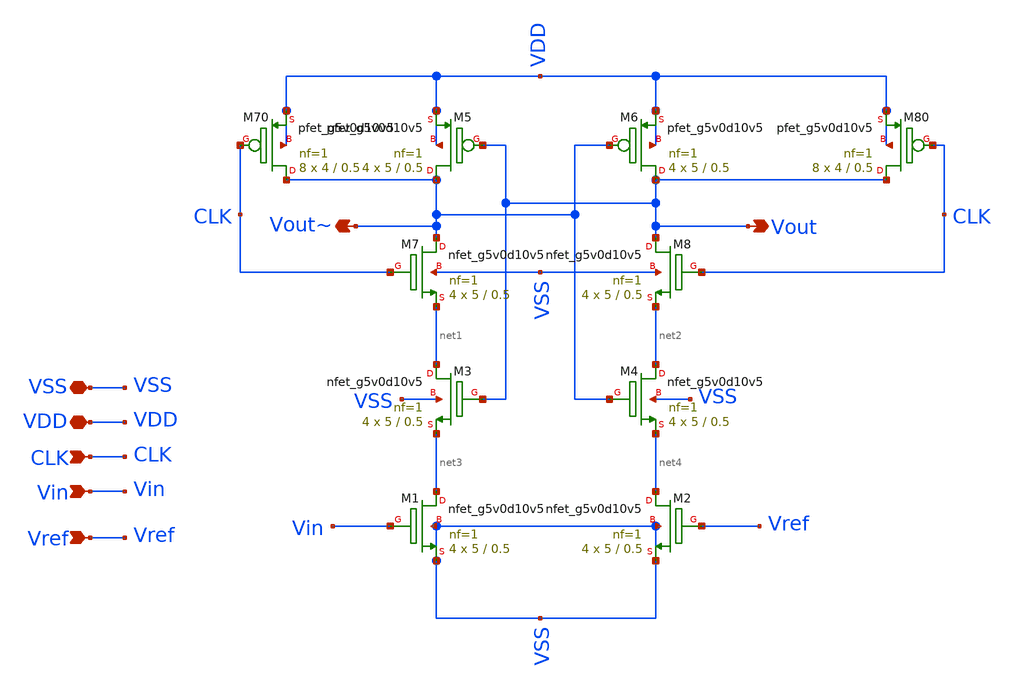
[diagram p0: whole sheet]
** sch_path: xschem/Amplifiers/StrongARM.sch
**.subckt StrongARM Vout~ Vout CLK Vin Vref VSS VDD
*.opin Vout~
*.opin Vout
*.ipin CLK
*.ipin Vin
*.ipin Vref
*.iopin VSS
*.iopin VDD
XM1 net3 Vin VSS VSS sky130_fd_pr__nfet_g5v0d10v5 L=0.5 W=5 nf=1 ad='int((nf+1)/2) * W/nf * 0.29' as='int((nf+2)/2) * W/nf * 0.29'
+ pd='2*int((nf+1)/2) * (W/nf + 0.29)' ps='2*int((nf+2)/2) * (W/nf + 0.29)' nrd='0.29 / W' nrs='0.29 / W'
+ sa=0 sb=0 sd=0 mult=4 m=4
XM2 net4 Vref VSS VSS sky130_fd_pr__nfet_g5v0d10v5 L=0.5 W=5 nf=1 ad='int((nf+1)/2) * W/nf * 0.29' as='int((nf+2)/2) * W/nf * 0.29'
+ pd='2*int((nf+1)/2) * (W/nf + 0.29)' ps='2*int((nf+2)/2) * (W/nf + 0.29)' nrd='0.29 / W' nrs='0.29 / W'
+ sa=0 sb=0 sd=0 mult=4 m=4
XM3 net1 Vout net3 VSS sky130_fd_pr__nfet_g5v0d10v5 L=0.5 W=5 nf=1 ad='int((nf+1)/2) * W/nf * 0.29' as='int((nf+2)/2) * W/nf * 0.29'
+ pd='2*int((nf+1)/2) * (W/nf + 0.29)' ps='2*int((nf+2)/2) * (W/nf + 0.29)' nrd='0.29 / W' nrs='0.29 / W'
+ sa=0 sb=0 sd=0 mult=4 m=4
XM4 net2 Vout~ net4 VSS sky130_fd_pr__nfet_g5v0d10v5 L=0.5 W=5 nf=1 ad='int((nf+1)/2) * W/nf * 0.29'
+ as='int((nf+2)/2) * W/nf * 0.29' pd='2*int((nf+1)/2) * (W/nf + 0.29)' ps='2*int((nf+2)/2) * (W/nf + 0.29)'
+ nrd='0.29 / W' nrs='0.29 / W' sa=0 sb=0 sd=0 mult=4 m=4
XM7 Vout~ CLK net1 VSS sky130_fd_pr__nfet_g5v0d10v5 L=0.5 W=5 nf=1 ad='int((nf+1)/2) * W/nf * 0.29' as='int((nf+2)/2) * W/nf * 0.29'
+ pd='2*int((nf+1)/2) * (W/nf + 0.29)' ps='2*int((nf+2)/2) * (W/nf + 0.29)' nrd='0.29 / W' nrs='0.29 / W'
+ sa=0 sb=0 sd=0 mult=4 m=4
XM8 Vout CLK net2 VSS sky130_fd_pr__nfet_g5v0d10v5 L=0.5 W=5 nf=1 ad='int((nf+1)/2) * W/nf * 0.29' as='int((nf+2)/2) * W/nf * 0.29'
+ pd='2*int((nf+1)/2) * (W/nf + 0.29)' ps='2*int((nf+2)/2) * (W/nf + 0.29)' nrd='0.29 / W' nrs='0.29 / W'
+ sa=0 sb=0 sd=0 mult=4 m=4
XM70 Vout~ CLK VDD VDD sky130_fd_pr__pfet_g5v0d10v5 L=0.5 W=4 nf=1 ad='int((nf+1)/2) * W/nf * 0.29' as='int((nf+2)/2) * W/nf * 0.29'
+ pd='2*int((nf+1)/2) * (W/nf + 0.29)' ps='2*int((nf+2)/2) * (W/nf + 0.29)' nrd='0.29 / W' nrs='0.29 / W'
+ sa=0 sb=0 sd=0 mult=8 m=8
XM80 Vout CLK VDD VDD sky130_fd_pr__pfet_g5v0d10v5 L=0.5 W=4 nf=1 ad='int((nf+1)/2) * W/nf * 0.29' as='int((nf+2)/2) * W/nf * 0.29'
+ pd='2*int((nf+1)/2) * (W/nf + 0.29)' ps='2*int((nf+2)/2) * (W/nf + 0.29)' nrd='0.29 / W' nrs='0.29 / W'
+ sa=0 sb=0 sd=0 mult=8 m=8
XM5 Vout~ Vout VDD VDD sky130_fd_pr__pfet_g5v0d10v5 L=0.5 W=5 nf=1 ad='int((nf+1)/2) * W/nf * 0.29' as='int((nf+2)/2) * W/nf * 0.29'
+ pd='2*int((nf+1)/2) * (W/nf + 0.29)' ps='2*int((nf+2)/2) * (W/nf + 0.29)' nrd='0.29 / W' nrs='0.29 / W'
+ sa=0 sb=0 sd=0 mult=4 m=4
XM6 Vout Vout~ VDD VDD sky130_fd_pr__pfet_g5v0d10v5 L=0.5 W=5 nf=1 ad='int((nf+1)/2) * W/nf * 0.29' as='int((nf+2)/2) * W/nf * 0.29'
+ pd='2*int((nf+1)/2) * (W/nf + 0.29)' ps='2*int((nf+2)/2) * (W/nf + 0.29)' nrd='0.29 / W' nrs='0.29 / W'
+ sa=0 sb=0 sd=0 mult=4 m=4
**.ends
.end
